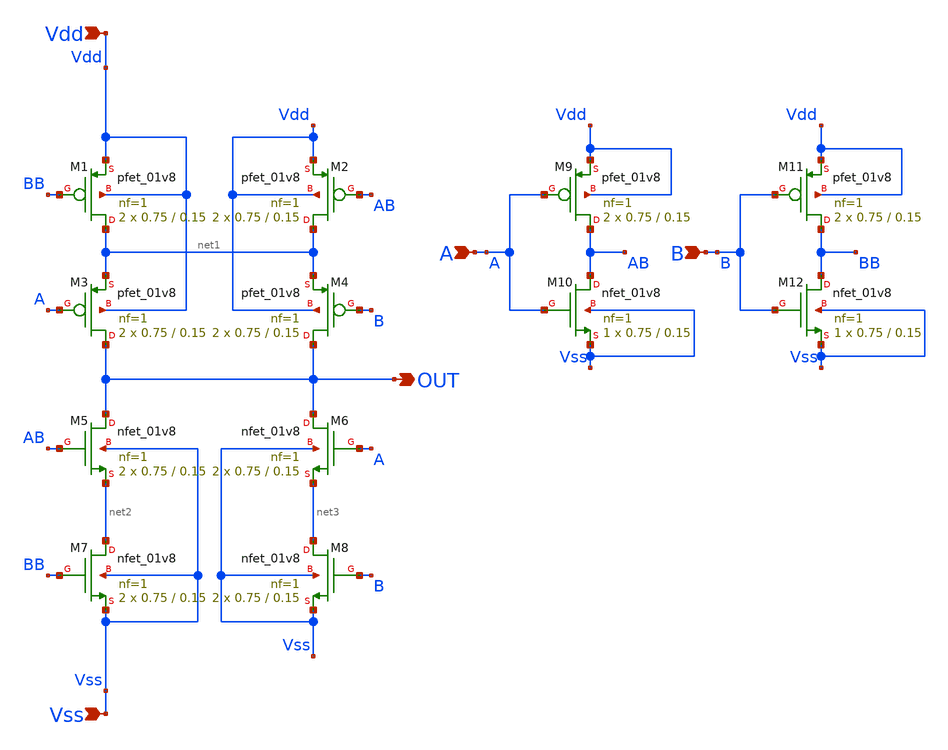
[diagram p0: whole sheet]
** sch_path: icdesign/sch/Xor/XOR.sch
**.subckt XOR Vdd Vss A B OUT
*.ipin Vdd
*.ipin Vss
*.ipin A
*.ipin B
*.opin OUT
XM1 net1 BB Vdd Vdd sky130_fd_pr__pfet_01v8 L=0.15 W=0.75 nf=1 ad='int((nf+1)/2) * W/nf * 0.29' as='int((nf+2)/2) * W/nf * 0.29'
+ pd='2*int((nf+1)/2) * (W/nf + 0.29)' ps='2*int((nf+2)/2) * (W/nf + 0.29)' nrd='0.29 / W' nrs='0.29 / W'
+ sa=0 sb=0 sd=0 mult=2 m=2
XM2 net1 AB Vdd Vdd sky130_fd_pr__pfet_01v8 L=0.15 W=0.75 nf=1 ad='int((nf+1)/2) * W/nf * 0.29' as='int((nf+2)/2) * W/nf * 0.29'
+ pd='2*int((nf+1)/2) * (W/nf + 0.29)' ps='2*int((nf+2)/2) * (W/nf + 0.29)' nrd='0.29 / W' nrs='0.29 / W'
+ sa=0 sb=0 sd=0 mult=2 m=2
XM3 OUT A net1 Vdd sky130_fd_pr__pfet_01v8 L=0.15 W=0.75 nf=1 ad='int((nf+1)/2) * W/nf * 0.29' as='int((nf+2)/2) * W/nf * 0.29'
+ pd='2*int((nf+1)/2) * (W/nf + 0.29)' ps='2*int((nf+2)/2) * (W/nf + 0.29)' nrd='0.29 / W' nrs='0.29 / W'
+ sa=0 sb=0 sd=0 mult=2 m=2
XM4 OUT B net1 Vdd sky130_fd_pr__pfet_01v8 L=0.15 W=0.75 nf=1 ad='int((nf+1)/2) * W/nf * 0.29' as='int((nf+2)/2) * W/nf * 0.29'
+ pd='2*int((nf+1)/2) * (W/nf + 0.29)' ps='2*int((nf+2)/2) * (W/nf + 0.29)' nrd='0.29 / W' nrs='0.29 / W'
+ sa=0 sb=0 sd=0 mult=2 m=2
XM5 OUT AB net2 Vss sky130_fd_pr__nfet_01v8 L=0.15 W=0.75 nf=1 ad='int((nf+1)/2) * W/nf * 0.29' as='int((nf+2)/2) * W/nf * 0.29'
+ pd='2*int((nf+1)/2) * (W/nf + 0.29)' ps='2*int((nf+2)/2) * (W/nf + 0.29)' nrd='0.29 / W' nrs='0.29 / W'
+ sa=0 sb=0 sd=0 mult=2 m=2
XM6 OUT A net3 Vss sky130_fd_pr__nfet_01v8 L=0.15 W=0.75 nf=1 ad='int((nf+1)/2) * W/nf * 0.29' as='int((nf+2)/2) * W/nf * 0.29'
+ pd='2*int((nf+1)/2) * (W/nf + 0.29)' ps='2*int((nf+2)/2) * (W/nf + 0.29)' nrd='0.29 / W' nrs='0.29 / W'
+ sa=0 sb=0 sd=0 mult=2 m=2
XM7 net2 BB Vss Vss sky130_fd_pr__nfet_01v8 L=0.15 W=0.75 nf=1 ad='int((nf+1)/2) * W/nf * 0.29' as='int((nf+2)/2) * W/nf * 0.29'
+ pd='2*int((nf+1)/2) * (W/nf + 0.29)' ps='2*int((nf+2)/2) * (W/nf + 0.29)' nrd='0.29 / W' nrs='0.29 / W'
+ sa=0 sb=0 sd=0 mult=2 m=2
XM8 net3 B Vss Vss sky130_fd_pr__nfet_01v8 L=0.15 W=0.75 nf=1 ad='int((nf+1)/2) * W/nf * 0.29' as='int((nf+2)/2) * W/nf * 0.29'
+ pd='2*int((nf+1)/2) * (W/nf + 0.29)' ps='2*int((nf+2)/2) * (W/nf + 0.29)' nrd='0.29 / W' nrs='0.29 / W'
+ sa=0 sb=0 sd=0 mult=2 m=2
XM9 AB A Vdd Vdd sky130_fd_pr__pfet_01v8 L=0.15 W=0.75 nf=1 ad='int((nf+1)/2) * W/nf * 0.29' as='int((nf+2)/2) * W/nf * 0.29'
+ pd='2*int((nf+1)/2) * (W/nf + 0.29)' ps='2*int((nf+2)/2) * (W/nf + 0.29)' nrd='0.29 / W' nrs='0.29 / W'
+ sa=0 sb=0 sd=0 mult=2 m=2
XM10 AB A Vss Vss sky130_fd_pr__nfet_01v8 L=0.15 W=0.75 nf=1 ad='int((nf+1)/2) * W/nf * 0.29' as='int((nf+2)/2) * W/nf * 0.29'
+ pd='2*int((nf+1)/2) * (W/nf + 0.29)' ps='2*int((nf+2)/2) * (W/nf + 0.29)' nrd='0.29 / W' nrs='0.29 / W'
+ sa=0 sb=0 sd=0 mult=1 m=1
XM11 BB B Vdd Vdd sky130_fd_pr__pfet_01v8 L=0.15 W=0.75 nf=1 ad='int((nf+1)/2) * W/nf * 0.29' as='int((nf+2)/2) * W/nf * 0.29'
+ pd='2*int((nf+1)/2) * (W/nf + 0.29)' ps='2*int((nf+2)/2) * (W/nf + 0.29)' nrd='0.29 / W' nrs='0.29 / W'
+ sa=0 sb=0 sd=0 mult=2 m=2
XM12 BB B Vss Vss sky130_fd_pr__nfet_01v8 L=0.15 W=0.75 nf=1 ad='int((nf+1)/2) * W/nf * 0.29' as='int((nf+2)/2) * W/nf * 0.29'
+ pd='2*int((nf+1)/2) * (W/nf + 0.29)' ps='2*int((nf+2)/2) * (W/nf + 0.29)' nrd='0.29 / W' nrs='0.29 / W'
+ sa=0 sb=0 sd=0 mult=1 m=1
**.ends
.end
